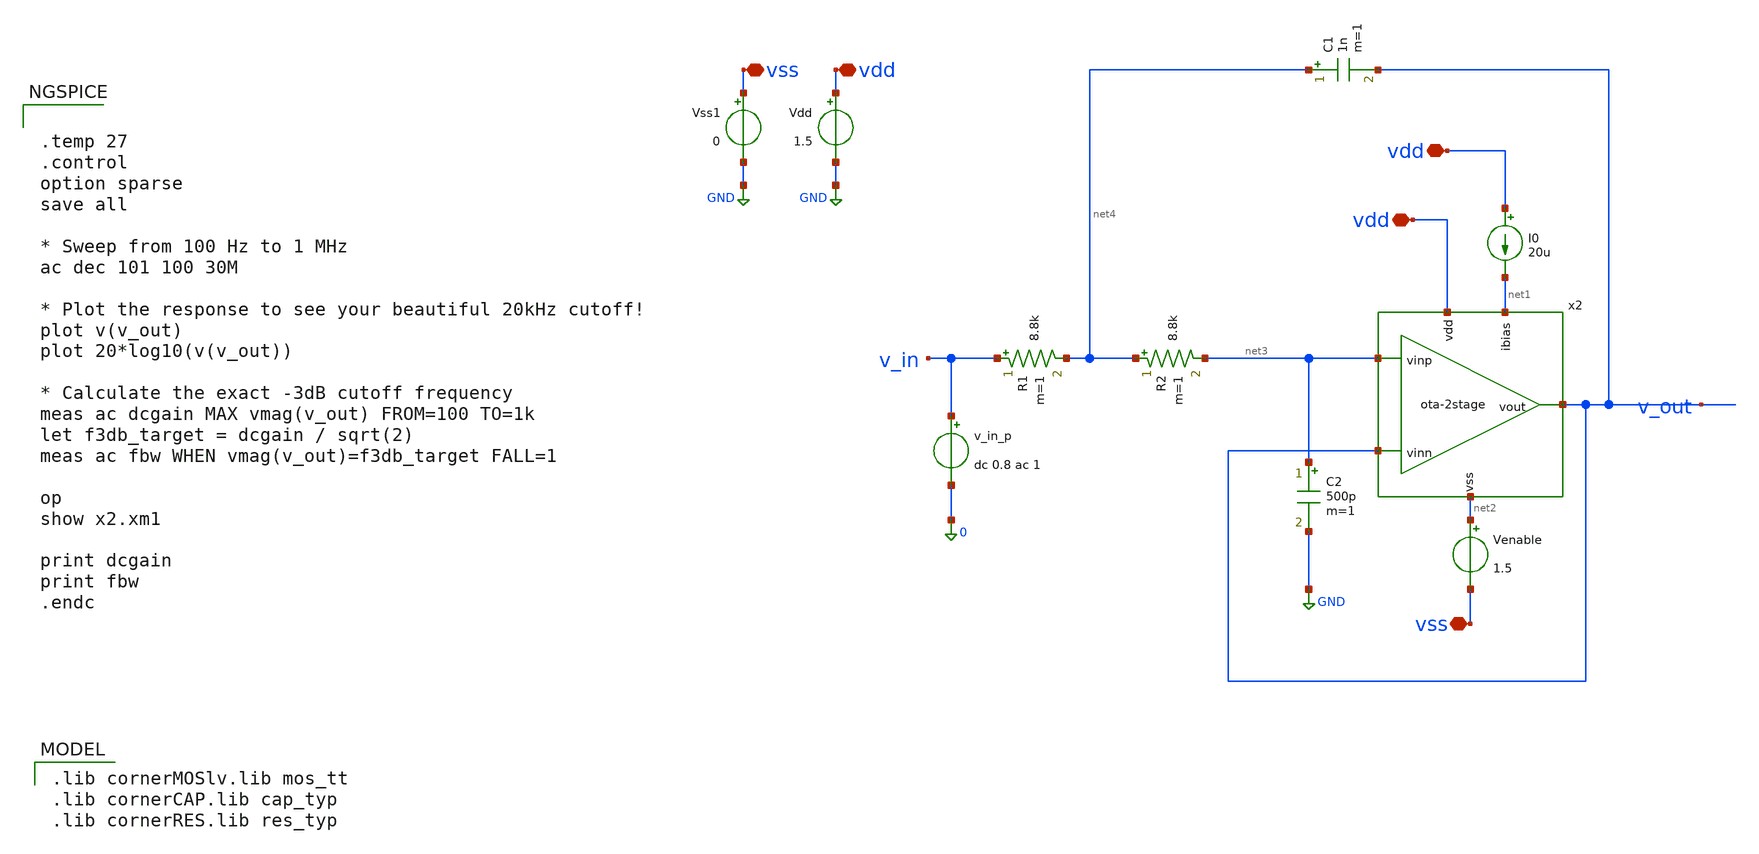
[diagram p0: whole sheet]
** sch_path: ota-2stage_tb-sk-lpf.sch
**.subckt ota-2stage_tb-sk-lpf vdd vdd vss vdd vss
*.iopin vdd
*.iopin vdd
*.iopin vss
*.iopin vdd
*.iopin vss
I0 vdd net1 20u
Venable net2 vss 1.5
v_in_p v_in 0 dc 0.8 ac 1
R1 v_in net4 8.8k m=1
R2 net4 net3 8.8k m=1
C2 net3 GND 500p m=1
C1 net4 v_out 1n m=1
x2 vdd net1 v_out v_out net3 net2 ota-2stage
Vdd vdd GND 1.5
Vss1 vss GND 0
**** begin user architecture code


.temp 27
.control
option sparse
save all

* Sweep from 100 Hz to 1 MHz
ac dec 101 100 30M

* Plot the response to see your beautiful 20kHz cutoff!
plot v(v_out)
plot 20*log10(v(v_out))

* Calculate the exact -3dB cutoff frequency
meas ac dcgain MAX vmag(v_out) FROM=100 TO=1k
let f3db_target = dcgain / sqrt(2)
meas ac fbw WHEN vmag(v_out)=f3db_target FALL=1

op
show x2.xm1

print dcgain
print fbw
.endc


 .lib cornerMOSlv.lib mos_tt
.lib cornerCAP.lib cap_typ
.lib cornerRES.lib res_typ

**** end user architecture code
**.ends
.GLOBAL GND
.end
